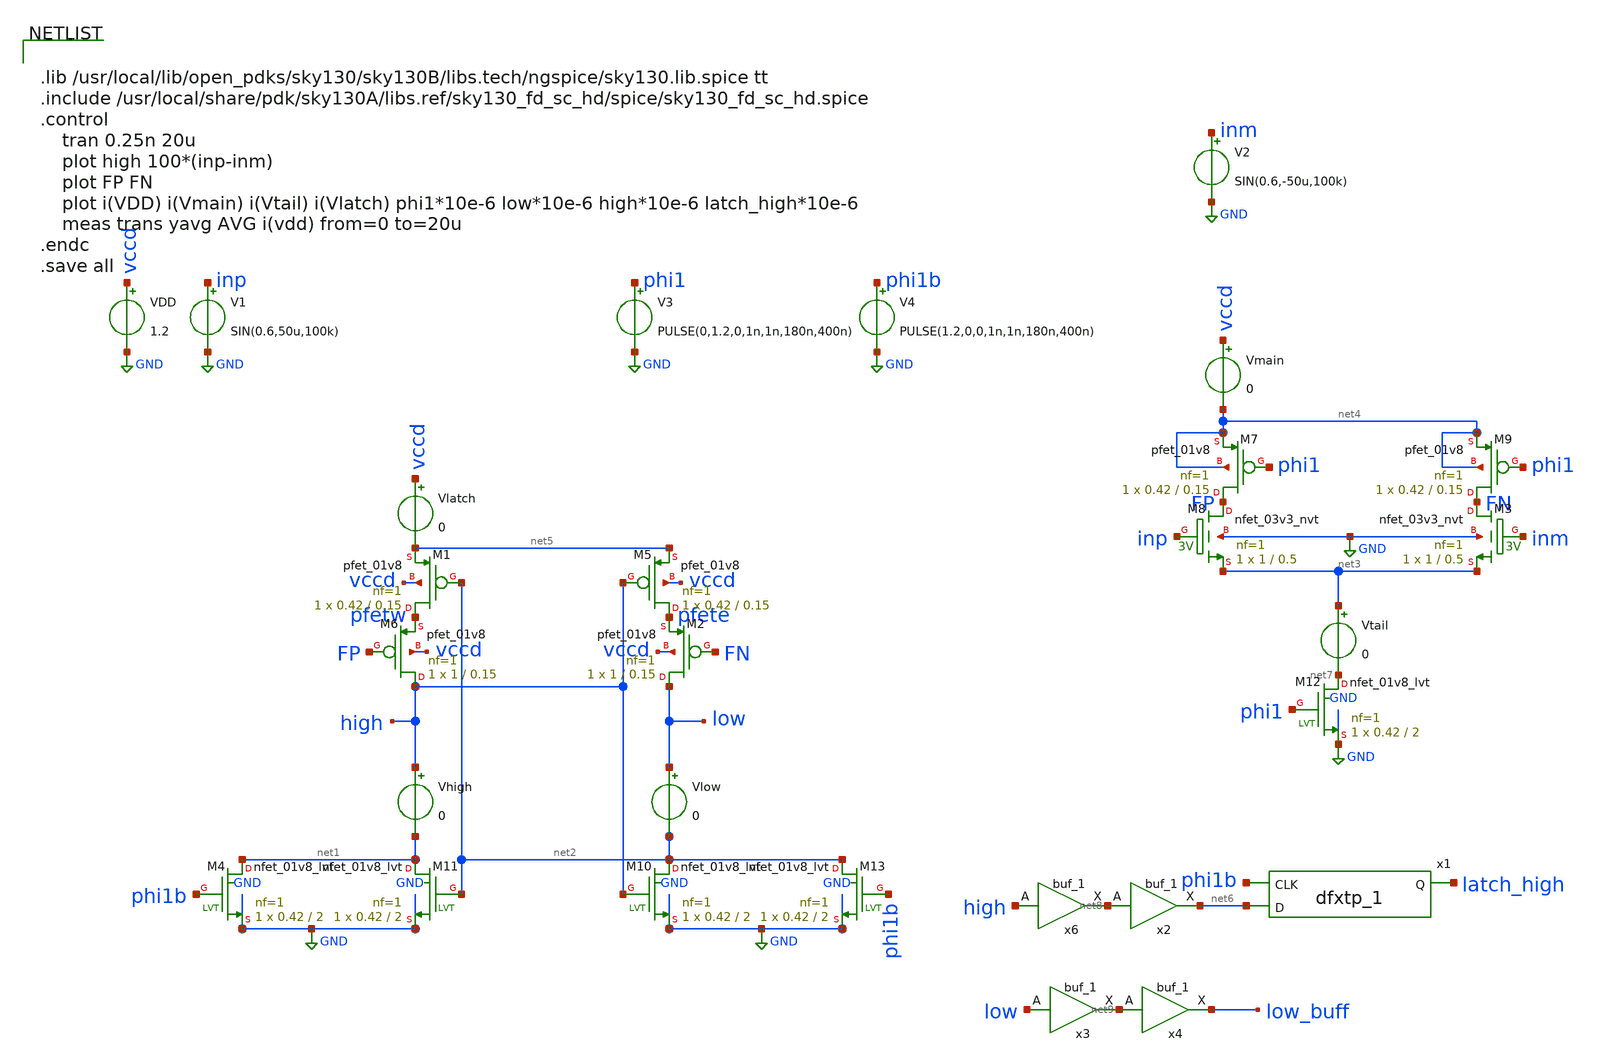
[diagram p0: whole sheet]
** sch_path: xschem/test_bench/comparator_tb.sch
**.subckt comparator_tb
V1 inp GND SIN(0.6,50u,100k)
VDD vccd GND 1.2
V2 inm GND SIN(0.6,-50u,100k)
V3 phi1 GND PULSE(0,1.2,0,1n,1n,180n,400n)
V4 phi1b GND PULSE(1.2,0,0,1n,1n,180n,400n)
Vtail net3 net7 0
Vmain vccd net4 0
Vlatch vccd net5 0
Vhigh high net1 0
Vlow low net2 0
x1 phi1b net6 GND GND vccd vccd latch_high sky130_fd_sc_hd__dfxtp_1
XM6 high FP pfetw vccd sky130_fd_pr__pfet_01v8 L=0.15 W=1 nf=1 ad='int((nf+1)/2) * W/nf * 0.29' as='int((nf+2)/2) * W/nf * 0.29'
+ pd='2*int((nf+1)/2) * (W/nf + 0.29)' ps='2*int((nf+2)/2) * (W/nf + 0.29)' nrd='0.29 / W' nrs='0.29 / W'
+ sa=0 sb=0 sd=0 mult=1 m=1
XM2 low FN pfete vccd sky130_fd_pr__pfet_01v8 L=0.15 W=1 nf=1 ad='int((nf+1)/2) * W/nf * 0.29' as='int((nf+2)/2) * W/nf * 0.29'
+ pd='2*int((nf+1)/2) * (W/nf + 0.29)' ps='2*int((nf+2)/2) * (W/nf + 0.29)' nrd='0.29 / W' nrs='0.29 / W'
+ sa=0 sb=0 sd=0 mult=1 m=1
XM1 pfetw net2 net5 vccd sky130_fd_pr__pfet_01v8 L=0.15 W=0.42 nf=1 ad='int((nf+1)/2) * W/nf * 0.29'
+ as='int((nf+2)/2) * W/nf * 0.29' pd='2*int((nf+1)/2) * (W/nf + 0.29)' ps='2*int((nf+2)/2) * (W/nf + 0.29)'
+ nrd='0.29 / W' nrs='0.29 / W' sa=0 sb=0 sd=0 mult=1 m=1
XM5 pfete high net5 vccd sky130_fd_pr__pfet_01v8 L=0.15 W=0.42 nf=1 ad='int((nf+1)/2) * W/nf * 0.29'
+ as='int((nf+2)/2) * W/nf * 0.29' pd='2*int((nf+1)/2) * (W/nf + 0.29)' ps='2*int((nf+2)/2) * (W/nf + 0.29)'
+ nrd='0.29 / W' nrs='0.29 / W' sa=0 sb=0 sd=0 mult=1 m=1
XM7 FP phi1 net4 net4 sky130_fd_pr__pfet_01v8 L=0.15 W=0.42 nf=1 ad='int((nf+1)/2) * W/nf * 0.29' as='int((nf+2)/2) * W/nf * 0.29'
+ pd='2*int((nf+1)/2) * (W/nf + 0.29)' ps='2*int((nf+2)/2) * (W/nf + 0.29)' nrd='0.29 / W' nrs='0.29 / W'
+ sa=0 sb=0 sd=0 mult=1 m=1
XM9 FN phi1 net4 net4 sky130_fd_pr__pfet_01v8 L=0.15 W=0.42 nf=1 ad='int((nf+1)/2) * W/nf * 0.29' as='int((nf+2)/2) * W/nf * 0.29'
+ pd='2*int((nf+1)/2) * (W/nf + 0.29)' ps='2*int((nf+2)/2) * (W/nf + 0.29)' nrd='0.29 / W' nrs='0.29 / W'
+ sa=0 sb=0 sd=0 mult=1 m=1
x6 high gnd gnd vccd vccd net8 sky130_fd_sc_hd__buf_1
x3 low gnd gnd vccd vccd net9 sky130_fd_sc_hd__buf_1
XM3 FN inm net3 GND sky130_fd_pr__nfet_03v3_nvt L=0.5 W=1 nf=1 ad='int((nf+1)/2) * W/nf * 0.29' as='int((nf+2)/2) * W/nf * 0.29'
+ pd='2*int((nf+1)/2) * (W/nf + 0.29)' ps='2*int((nf+2)/2) * (W/nf + 0.29)' nrd='0.29 / W' nrs='0.29 / W'
+ sa=0 sb=0 sd=0 mult=1 m=1
XM8 FP inp net3 GND sky130_fd_pr__nfet_03v3_nvt L=0.5 W=1 nf=1 ad='int((nf+1)/2) * W/nf * 0.29' as='int((nf+2)/2) * W/nf * 0.29'
+ pd='2*int((nf+1)/2) * (W/nf + 0.29)' ps='2*int((nf+2)/2) * (W/nf + 0.29)' nrd='0.29 / W' nrs='0.29 / W'
+ sa=0 sb=0 sd=0 mult=1 m=1
XM4 net1 phi1b GND GND sky130_fd_pr__nfet_01v8_lvt L=2 W=0.42 nf=1 ad='int((nf+1)/2) * W/nf * 0.29' as='int((nf+2)/2) * W/nf * 0.29'
+ pd='2*int((nf+1)/2) * (W/nf + 0.29)' ps='2*int((nf+2)/2) * (W/nf + 0.29)' nrd='0.29 / W' nrs='0.29 / W'
+ sa=0 sb=0 sd=0 mult=1 m=1
XM10 net2 high GND GND sky130_fd_pr__nfet_01v8_lvt L=2 W=0.42 nf=1 ad='int((nf+1)/2) * W/nf * 0.29' as='int((nf+2)/2) * W/nf * 0.29'
+ pd='2*int((nf+1)/2) * (W/nf + 0.29)' ps='2*int((nf+2)/2) * (W/nf + 0.29)' nrd='0.29 / W' nrs='0.29 / W'
+ sa=0 sb=0 sd=0 mult=1 m=1
XM12 net7 phi1 GND GND sky130_fd_pr__nfet_01v8_lvt L=2 W=0.42 nf=1 ad='int((nf+1)/2) * W/nf * 0.29' as='int((nf+2)/2) * W/nf * 0.29'
+ pd='2*int((nf+1)/2) * (W/nf + 0.29)' ps='2*int((nf+2)/2) * (W/nf + 0.29)' nrd='0.29 / W' nrs='0.29 / W'
+ sa=0 sb=0 sd=0 mult=1 m=1
XM11 net1 net2 GND GND sky130_fd_pr__nfet_01v8_lvt L=2 W=0.42 nf=1 ad='int((nf+1)/2) * W/nf * 0.29' as='int((nf+2)/2) * W/nf * 0.29'
+ pd='2*int((nf+1)/2) * (W/nf + 0.29)' ps='2*int((nf+2)/2) * (W/nf + 0.29)' nrd='0.29 / W' nrs='0.29 / W'
+ sa=0 sb=0 sd=0 mult=1 m=1
XM13 net2 phi1b GND GND sky130_fd_pr__nfet_01v8_lvt L=2 W=0.42 nf=1 ad='int((nf+1)/2) * W/nf * 0.29'
+ as='int((nf+2)/2) * W/nf * 0.29' pd='2*int((nf+1)/2) * (W/nf + 0.29)' ps='2*int((nf+2)/2) * (W/nf + 0.29)'
+ nrd='0.29 / W' nrs='0.29 / W' sa=0 sb=0 sd=0 mult=1 m=1
x2 net8 gnd gnd vccd vccd net6 sky130_fd_sc_hd__buf_1
x4 net9 gnd gnd vccd vccd low_buff sky130_fd_sc_hd__buf_1
**** begin user architecture code


.lib /usr/local/lib/open_pdks/sky130/sky130B/libs.tech/ngspice/sky130.lib.spice tt
.include /usr/local/share/pdk/sky130A/libs.ref/sky130_fd_sc_hd/spice/sky130_fd_sc_hd.spice
.control
    tran 0.25n 20u
    plot high 100*(inp-inm)
    plot FP FN
    plot i(VDD) i(Vmain) i(Vtail) i(Vlatch) phi1*10e-6 low*10e-6 high*10e-6 latch_high*10e-6
    meas trans yavg AVG i(vdd) from=0 to=20u
.endc
.save all


**** end user architecture code
**.ends
.GLOBAL GND
.end
